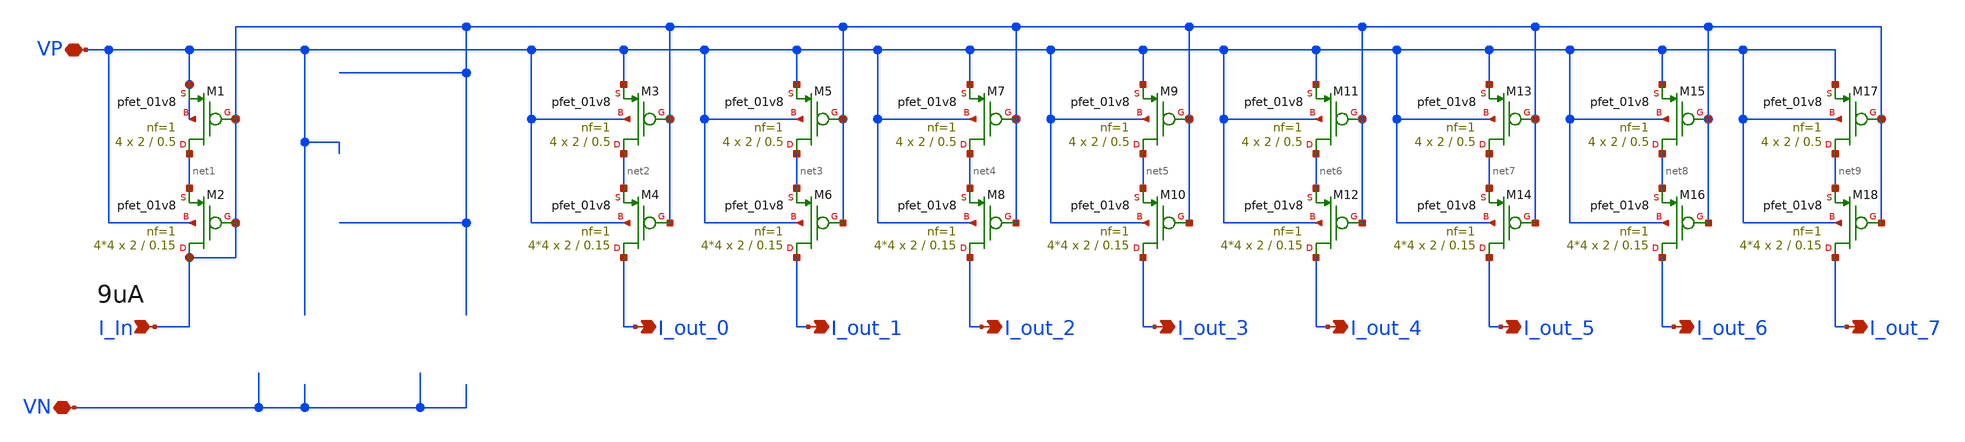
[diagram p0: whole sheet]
** sch_path: xschem/bias/current_mirrorx8.sch
**.subckt current_mirrorx8 I_out_0 I_In VP I_out_1 I_out_2 I_out_3 I_out_4 I_out_5 I_out_6 I_out_7
*+ VN
*.opin I_out_0
*.ipin I_In
*.iopin VP
*.opin I_out_1
*.opin I_out_2
*.opin I_out_3
*.opin I_out_4
*.opin I_out_5
*.opin I_out_6
*.opin I_out_7
*.iopin VN
XM1 net1 I_In VP VP sky130_fd_pr__pfet_01v8 L=0.5 W=2 nf=1 ad='int((nf+1)/2) * W/nf * 0.29' as='int((nf+2)/2) * W/nf * 0.29'
+ pd='2*int((nf+1)/2) * (W/nf + 0.29)' ps='2*int((nf+2)/2) * (W/nf + 0.29)' nrd='0.29 / W' nrs='0.29 / W'
+ sa=0 sb=0 sd=0 mult=4 m=4
XM2 I_In I_In net1 VP sky130_fd_pr__pfet_01v8 L=0.15 W=2 nf=1 ad='int((nf+1)/2) * W/nf * 0.29' as='int((nf+2)/2) * W/nf * 0.29'
+ pd='2*int((nf+1)/2) * (W/nf + 0.29)' ps='2*int((nf+2)/2) * (W/nf + 0.29)' nrd='0.29 / W' nrs='0.29 / W'
+ sa=0 sb=0 sd=0 mult=4*4 m=4*4
XM3 net2 I_In VP VP sky130_fd_pr__pfet_01v8 L=0.5 W=2 nf=1 ad='int((nf+1)/2) * W/nf * 0.29' as='int((nf+2)/2) * W/nf * 0.29'
+ pd='2*int((nf+1)/2) * (W/nf + 0.29)' ps='2*int((nf+2)/2) * (W/nf + 0.29)' nrd='0.29 / W' nrs='0.29 / W'
+ sa=0 sb=0 sd=0 mult=4 m=4
XM4 I_out_0 I_In net2 VP sky130_fd_pr__pfet_01v8 L=0.15 W=2 nf=1 ad='int((nf+1)/2) * W/nf * 0.29' as='int((nf+2)/2) * W/nf * 0.29'
+ pd='2*int((nf+1)/2) * (W/nf + 0.29)' ps='2*int((nf+2)/2) * (W/nf + 0.29)' nrd='0.29 / W' nrs='0.29 / W'
+ sa=0 sb=0 sd=0 mult=4*4 m=4*4
XM5 net3 I_In VP VP sky130_fd_pr__pfet_01v8 L=0.5 W=2 nf=1 ad='int((nf+1)/2) * W/nf * 0.29' as='int((nf+2)/2) * W/nf * 0.29'
+ pd='2*int((nf+1)/2) * (W/nf + 0.29)' ps='2*int((nf+2)/2) * (W/nf + 0.29)' nrd='0.29 / W' nrs='0.29 / W'
+ sa=0 sb=0 sd=0 mult=4 m=4
XM6 I_out_1 I_In net3 VP sky130_fd_pr__pfet_01v8 L=0.15 W=2 nf=1 ad='int((nf+1)/2) * W/nf * 0.29' as='int((nf+2)/2) * W/nf * 0.29'
+ pd='2*int((nf+1)/2) * (W/nf + 0.29)' ps='2*int((nf+2)/2) * (W/nf + 0.29)' nrd='0.29 / W' nrs='0.29 / W'
+ sa=0 sb=0 sd=0 mult=4*4 m=4*4
XM7 net4 I_In VP VP sky130_fd_pr__pfet_01v8 L=0.5 W=2 nf=1 ad='int((nf+1)/2) * W/nf * 0.29' as='int((nf+2)/2) * W/nf * 0.29'
+ pd='2*int((nf+1)/2) * (W/nf + 0.29)' ps='2*int((nf+2)/2) * (W/nf + 0.29)' nrd='0.29 / W' nrs='0.29 / W'
+ sa=0 sb=0 sd=0 mult=4 m=4
XM8 I_out_2 I_In net4 VP sky130_fd_pr__pfet_01v8 L=0.15 W=2 nf=1 ad='int((nf+1)/2) * W/nf * 0.29' as='int((nf+2)/2) * W/nf * 0.29'
+ pd='2*int((nf+1)/2) * (W/nf + 0.29)' ps='2*int((nf+2)/2) * (W/nf + 0.29)' nrd='0.29 / W' nrs='0.29 / W'
+ sa=0 sb=0 sd=0 mult=4*4 m=4*4
XM9 net5 I_In VP VP sky130_fd_pr__pfet_01v8 L=0.5 W=2 nf=1 ad='int((nf+1)/2) * W/nf * 0.29' as='int((nf+2)/2) * W/nf * 0.29'
+ pd='2*int((nf+1)/2) * (W/nf + 0.29)' ps='2*int((nf+2)/2) * (W/nf + 0.29)' nrd='0.29 / W' nrs='0.29 / W'
+ sa=0 sb=0 sd=0 mult=4 m=4
XM10 I_out_3 I_In net5 VP sky130_fd_pr__pfet_01v8 L=0.15 W=2 nf=1 ad='int((nf+1)/2) * W/nf * 0.29' as='int((nf+2)/2) * W/nf * 0.29'
+ pd='2*int((nf+1)/2) * (W/nf + 0.29)' ps='2*int((nf+2)/2) * (W/nf + 0.29)' nrd='0.29 / W' nrs='0.29 / W'
+ sa=0 sb=0 sd=0 mult=4*4 m=4*4
XM11 net6 I_In VP VP sky130_fd_pr__pfet_01v8 L=0.5 W=2 nf=1 ad='int((nf+1)/2) * W/nf * 0.29' as='int((nf+2)/2) * W/nf * 0.29'
+ pd='2*int((nf+1)/2) * (W/nf + 0.29)' ps='2*int((nf+2)/2) * (W/nf + 0.29)' nrd='0.29 / W' nrs='0.29 / W'
+ sa=0 sb=0 sd=0 mult=4 m=4
XM12 I_out_4 I_In net6 VP sky130_fd_pr__pfet_01v8 L=0.15 W=2 nf=1 ad='int((nf+1)/2) * W/nf * 0.29' as='int((nf+2)/2) * W/nf * 0.29'
+ pd='2*int((nf+1)/2) * (W/nf + 0.29)' ps='2*int((nf+2)/2) * (W/nf + 0.29)' nrd='0.29 / W' nrs='0.29 / W'
+ sa=0 sb=0 sd=0 mult=4*4 m=4*4
XM13 net7 I_In VP VP sky130_fd_pr__pfet_01v8 L=0.5 W=2 nf=1 ad='int((nf+1)/2) * W/nf * 0.29' as='int((nf+2)/2) * W/nf * 0.29'
+ pd='2*int((nf+1)/2) * (W/nf + 0.29)' ps='2*int((nf+2)/2) * (W/nf + 0.29)' nrd='0.29 / W' nrs='0.29 / W'
+ sa=0 sb=0 sd=0 mult=4 m=4
XM14 I_out_5 I_In net7 VP sky130_fd_pr__pfet_01v8 L=0.15 W=2 nf=1 ad='int((nf+1)/2) * W/nf * 0.29' as='int((nf+2)/2) * W/nf * 0.29'
+ pd='2*int((nf+1)/2) * (W/nf + 0.29)' ps='2*int((nf+2)/2) * (W/nf + 0.29)' nrd='0.29 / W' nrs='0.29 / W'
+ sa=0 sb=0 sd=0 mult=4*4 m=4*4
XM15 net8 I_In VP VP sky130_fd_pr__pfet_01v8 L=0.5 W=2 nf=1 ad='int((nf+1)/2) * W/nf * 0.29' as='int((nf+2)/2) * W/nf * 0.29'
+ pd='2*int((nf+1)/2) * (W/nf + 0.29)' ps='2*int((nf+2)/2) * (W/nf + 0.29)' nrd='0.29 / W' nrs='0.29 / W'
+ sa=0 sb=0 sd=0 mult=4 m=4
XM16 I_out_6 I_In net8 VP sky130_fd_pr__pfet_01v8 L=0.15 W=2 nf=1 ad='int((nf+1)/2) * W/nf * 0.29' as='int((nf+2)/2) * W/nf * 0.29'
+ pd='2*int((nf+1)/2) * (W/nf + 0.29)' ps='2*int((nf+2)/2) * (W/nf + 0.29)' nrd='0.29 / W' nrs='0.29 / W'
+ sa=0 sb=0 sd=0 mult=4*4 m=4*4
XM17 net9 I_In VP VP sky130_fd_pr__pfet_01v8 L=0.5 W=2 nf=1 ad='int((nf+1)/2) * W/nf * 0.29' as='int((nf+2)/2) * W/nf * 0.29'
+ pd='2*int((nf+1)/2) * (W/nf + 0.29)' ps='2*int((nf+2)/2) * (W/nf + 0.29)' nrd='0.29 / W' nrs='0.29 / W'
+ sa=0 sb=0 sd=0 mult=4 m=4
XM18 I_out_7 I_In net9 VP sky130_fd_pr__pfet_01v8 L=0.15 W=2 nf=1 ad='int((nf+1)/2) * W/nf * 0.29' as='int((nf+2)/2) * W/nf * 0.29'
+ pd='2*int((nf+1)/2) * (W/nf + 0.29)' ps='2*int((nf+2)/2) * (W/nf + 0.29)' nrd='0.29 / W' nrs='0.29 / W'
+ sa=0 sb=0 sd=0 mult=4*4 m=4*4
**.ends
.end
